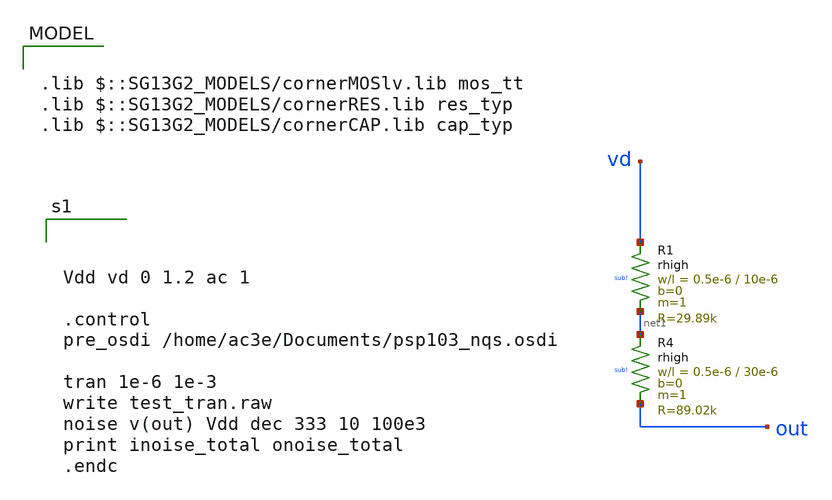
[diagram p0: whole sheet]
** sch_path: noise-test.sch
**.subckt noise-test
XR4 net1 out sub! rhigh w=0.5e-6 l=30e-6 m=1 b=0 mm_ok=1
XR1 vd net1 sub! rhigh w=0.5e-6 l=10e-6 m=1 b=0 mm_ok=1
**** begin user architecture code



Vdd vd 0 1.2 ac 1

.control
pre_osdi /home/ac3e/Documents/psp103_nqs.osdi

tran 1e-6 1e-3
write test_tran.raw
noise v(out) Vdd dec 333 10 100e3
print inoise_total onoise_total
.endc





.lib $::SG13G2_MODELS/cornerMOSlv.lib mos_tt
.lib $::SG13G2_MODELS/cornerRES.lib res_typ
.lib $::SG13G2_MODELS/cornerCAP.lib cap_typ

**** end user architecture code
**.ends
.end
